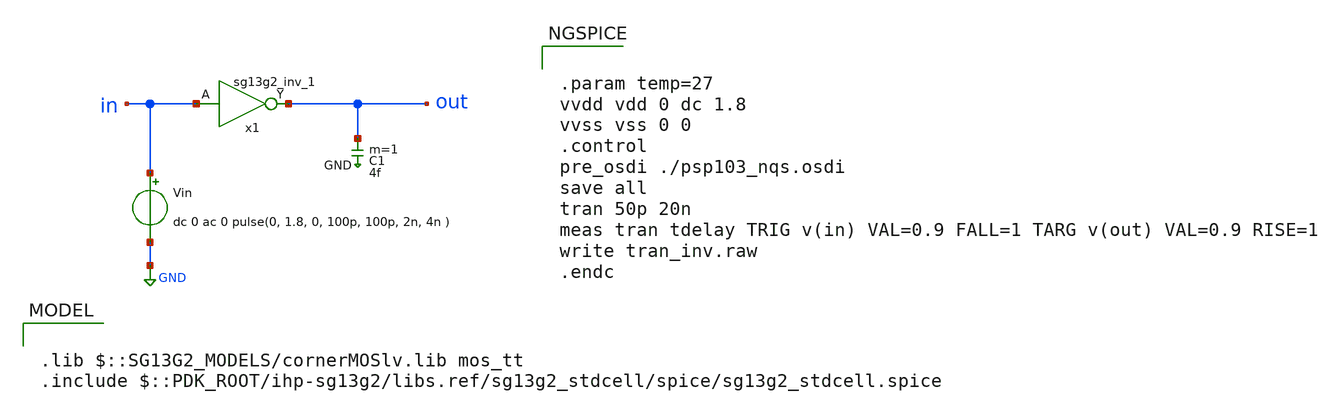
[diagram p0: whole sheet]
** sch_path: ihp-sg13g2/libs.tech/xschem/sg13g2_stdcells/tran_inv.sch
* Copyright 2024 IHP PDK Authors

.lib $::SG13G2_MODELS/cornerMOSlv.lib mos_tt
.include $::PDK_ROOT/ihp-sg13g2/libs.ref/sg13g2_stdcell/spice/sg13g2_stdcell.spice

**.subckt tran_inv
Vin in GND dc 0 ac 0 pulse(0, 1.8, 0, 100p, 100p, 2n, 4n )
x1 in VDD VSS out sg13g2_inv_1
C1 out GND 4f m=1
**** begin user architecture code


.param temp=27
vvdd vdd 0 dc 1.8
vvss vss 0 0
.control
pre_osdi ./psp103_nqs.osdi
save all
tran 50p 20n
meas tran tdelay TRIG v(in) VAL=0.9 FALL=1 TARG v(out) VAL=0.9 RISE=1
write tran_inv.raw
.endc


**** end user architecture code
**.ends
.GLOBAL GND
.end
